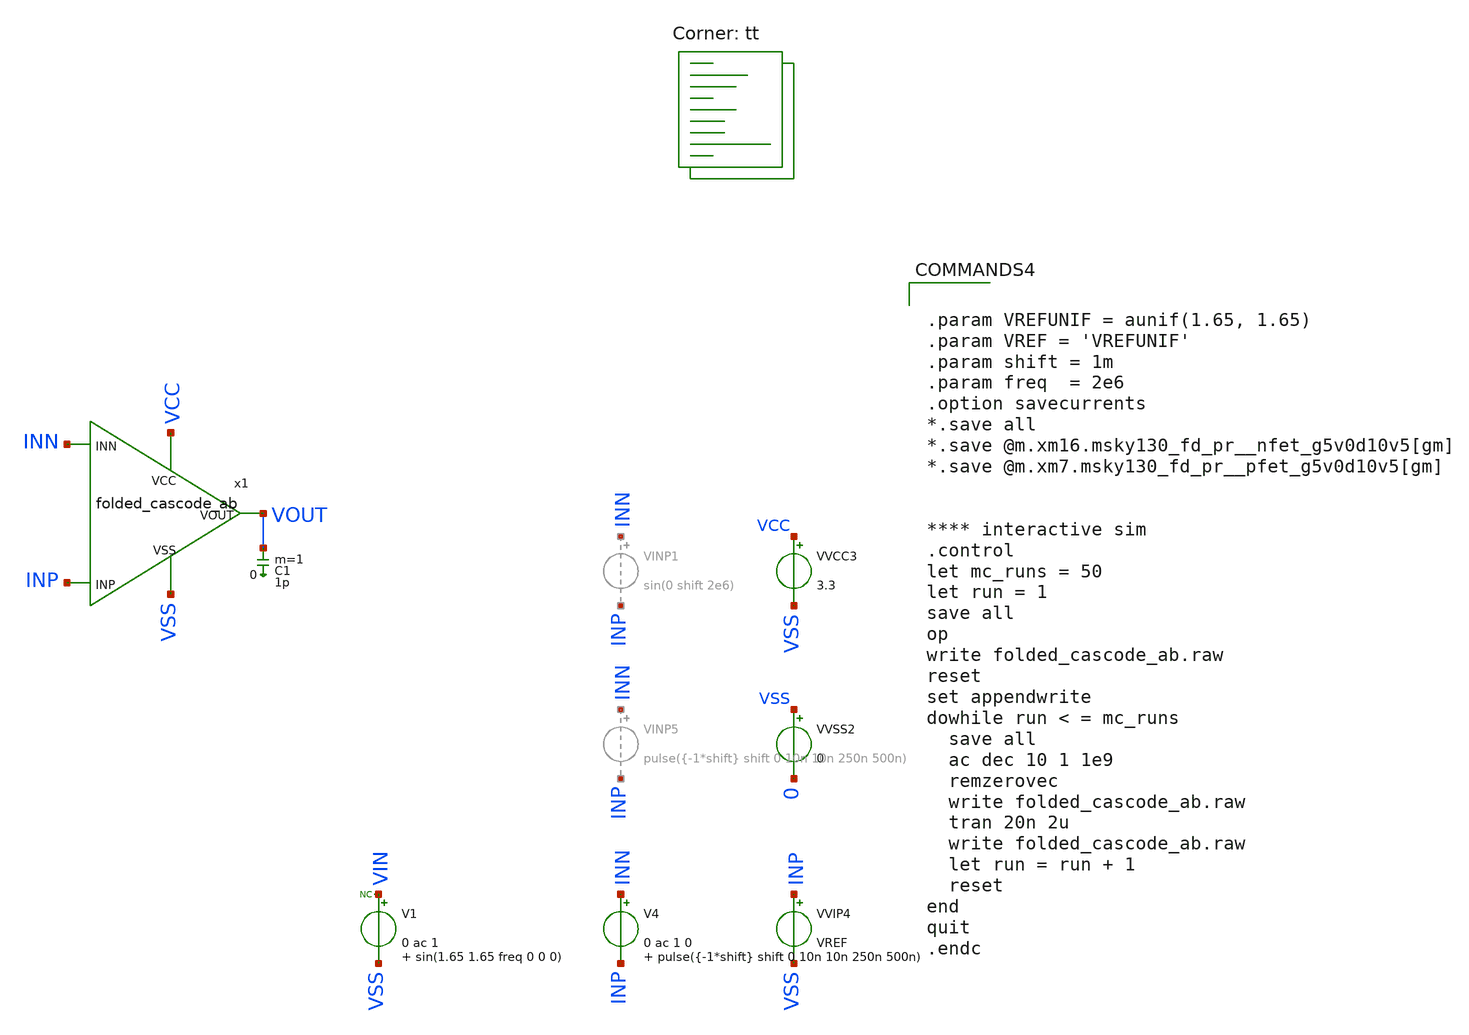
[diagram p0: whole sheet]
** sch_path: cadence_optimized/folded_cascode_ab_tb.sch
**.subckt folded_cascode_ab_tb
VVSS2 VSS 0 0
VVCC3 VCC VSS 3.3
VVIP4 INP VSS VREF
* noconn VIN
V1 VIN VSS 0 ac 1 sin(1.65 1.65 freq 0 0 0)
V4 INN INP 0 ac 1 0 pulse({-1*shift} shift 0 10n 10n 250n 500n)
x1 VSS VCC VOUT INN INP folded_cascode_ab
C1 VOUT 0 1p m=1
**** begin user architecture code
.lib $::SKYWATER_MODELS/sky130.lib.spice tt


.param VREFUNIF = aunif(1.65, 1.65)
.param VREF = 'VREFUNIF'
.param shift = 1m
.param freq  = 2e6
.option savecurrents
*.save all
*.save @m.xm16.msky130_fd_pr__nfet_g5v0d10v5[gm]
*.save @m.xm7.msky130_fd_pr__pfet_g5v0d10v5[gm]


**** interactive sim
.control
let mc_runs = 50
let run = 1
save all
op
write folded_cascode_ab.raw
reset
set appendwrite
dowhile run < = mc_runs
  save all
  ac dec 10 1 1e9
  remzerovec
  write folded_cascode_ab.raw
  tran 20n 2u
  write folded_cascode_ab.raw
  let run = run + 1
  reset
end
quit
.endc




**** end user architecture code
**.ends

* expanding   symbol:
*+  /foss/designs/Comparator/old/schematic/folded_cascode/backup/cadence_optimized/folded_cascode_ab.sym # of pins=5
** sym_path: cadence_optimized/folded_cascode_ab.sym
** sch_path: cadence_optimized/folded_cascode_ab.sch
.subckt folded_cascode_ab VSS VCC VOUT INN INP
*.iopin VCC
*.opin VOUT
*.ipin INN
*.ipin INP
*.iopin VSS
XM1 N4 net3 VSS VSS sky130_fd_pr__nfet_g5v0d10v5 L=0.5 W=4.5 nf=1 ad='int((nf+1)/2) * W/nf * 0.29' as='int((nf+2)/2) * W/nf * 0.29'
+ pd='2*int((nf+1)/2) * (W/nf + 0.29)' ps='2*int((nf+2)/2) * (W/nf + 0.29)' nrd='0.29 / W' nrs='0.29 / W'
+ sa=0 sb=0 sd=0 mult=1 m=1
XM2 out4 y N4 VSS sky130_fd_pr__nfet_g5v0d10v5 L=0.5 W=4 nf=1 ad='int((nf+1)/2) * W/nf * 0.29' as='int((nf+2)/2) * W/nf * 0.29'
+ pd='2*int((nf+1)/2) * (W/nf + 0.29)' ps='2*int((nf+2)/2) * (W/nf + 0.29)' nrd='0.29 / W' nrs='0.29 / W'
+ sa=0 sb=0 sd=0 mult=1 m=1
XM9 net3 y N3 VSS sky130_fd_pr__nfet_g5v0d10v5 L=0.5 W=4 nf=1 ad='int((nf+1)/2) * W/nf * 0.29' as='int((nf+2)/2) * W/nf * 0.29'
+ pd='2*int((nf+1)/2) * (W/nf + 0.29)' ps='2*int((nf+2)/2) * (W/nf + 0.29)' nrd='0.29 / W' nrs='0.29 / W'
+ sa=0 sb=0 sd=0 mult=1 m=1
XM10 N3 net3 VSS VSS sky130_fd_pr__nfet_g5v0d10v5 L=0.5 W=4.5 nf=1 ad='int((nf+1)/2) * W/nf * 0.29' as='int((nf+2)/2) * W/nf * 0.29'
+ pd='2*int((nf+1)/2) * (W/nf + 0.29)' ps='2*int((nf+2)/2) * (W/nf + 0.29)' nrd='0.29 / W' nrs='0.29 / W'
+ sa=0 sb=0 sd=0 mult=1 m=1
XM11 net1 out N1 VCC sky130_fd_pr__pfet_g5v0d10v5 L=0.5 W=4 nf=1 ad='int((nf+1)/2) * W/nf * 0.29' as='int((nf+2)/2) * W/nf * 0.29'
+ pd='2*int((nf+1)/2) * (W/nf + 0.29)' ps='2*int((nf+2)/2) * (W/nf + 0.29)' nrd='0.29 / W' nrs='0.29 / W'
+ sa=0 sb=0 sd=0 mult=1 m=1
XM12 out3 out N2 VCC sky130_fd_pr__pfet_g5v0d10v5 L=0.5 W=4 nf=1 ad='int((nf+1)/2) * W/nf * 0.29' as='int((nf+2)/2) * W/nf * 0.29'
+ pd='2*int((nf+1)/2) * (W/nf + 0.29)' ps='2*int((nf+2)/2) * (W/nf + 0.29)' nrd='0.29 / W' nrs='0.29 / W'
+ sa=0 sb=0 sd=0 mult=1 m=1
XM13 N1 net1 VCC VCC sky130_fd_pr__pfet_g5v0d10v5 L=0.5 W=2 nf=1 ad='int((nf+1)/2) * W/nf * 0.29' as='int((nf+2)/2) * W/nf * 0.29'
+ pd='2*int((nf+1)/2) * (W/nf + 0.29)' ps='2*int((nf+2)/2) * (W/nf + 0.29)' nrd='0.29 / W' nrs='0.29 / W'
+ sa=0 sb=0 sd=0 mult=1 m=1
XM14 N2 net1 VCC VCC sky130_fd_pr__pfet_g5v0d10v5 L=0.5 W=2 nf=1 ad='int((nf+1)/2) * W/nf * 0.29' as='int((nf+2)/2) * W/nf * 0.29'
+ pd='2*int((nf+1)/2) * (W/nf + 0.29)' ps='2*int((nf+2)/2) * (W/nf + 0.29)' nrd='0.29 / W' nrs='0.29 / W'
+ sa=0 sb=0 sd=0 mult=1 m=1
XM16 N2 INN net5 VSS sky130_fd_pr__nfet_g5v0d10v5 L=0.5 W=4 nf=1 ad='int((nf+1)/2) * W/nf * 0.29' as='int((nf+2)/2) * W/nf * 0.29'
+ pd='2*int((nf+1)/2) * (W/nf + 0.29)' ps='2*int((nf+2)/2) * (W/nf + 0.29)' nrd='0.29 / W' nrs='0.29 / W'
+ sa=0 sb=0 sd=0 mult=2 m=2
XM6 N4 INN net2 VCC sky130_fd_pr__pfet_g5v0d10v5 L=0.5 W=4 nf=1 ad='int((nf+1)/2) * W/nf * 0.29' as='int((nf+2)/2) * W/nf * 0.29'
+ pd='2*int((nf+1)/2) * (W/nf + 0.29)' ps='2*int((nf+2)/2) * (W/nf + 0.29)' nrd='0.29 / W' nrs='0.29 / W'
+ sa=0 sb=0 sd=0 mult=2 m=2
Vmeas2 net7 net2 0
.save i(vmeas2)
XM20 s s VCC VCC sky130_fd_pr__pfet_g5v0d10v5 L=0.5 W=0.5 nf=1 ad='int((nf+1)/2) * W/nf * 0.29' as='int((nf+2)/2) * W/nf * 0.29'
+ pd='2*int((nf+1)/2) * (W/nf + 0.29)' ps='2*int((nf+2)/2) * (W/nf + 0.29)' nrd='0.29 / W' nrs='0.29 / W'
+ sa=0 sb=0 sd=0 mult=1 m=1
XM21 p p s VCC sky130_fd_pr__pfet_g5v0d10v5 L=0.5 W=0.5 nf=1 ad='int((nf+1)/2) * W/nf * 0.29' as='int((nf+2)/2) * W/nf * 0.29'
+ pd='2*int((nf+1)/2) * (W/nf + 0.29)' ps='2*int((nf+2)/2) * (W/nf + 0.29)' nrd='0.29 / W' nrs='0.29 / W'
+ sa=0 sb=0 sd=0 mult=1 m=1
XM22 q q net4 VSS sky130_fd_pr__nfet_g5v0d10v5 L=0.5 W=1 nf=1 ad='int((nf+1)/2) * W/nf * 0.29' as='int((nf+2)/2) * W/nf * 0.29'
+ pd='2*int((nf+1)/2) * (W/nf + 0.29)' ps='2*int((nf+2)/2) * (W/nf + 0.29)' nrd='0.29 / W' nrs='0.29 / W'
+ sa=0 sb=0 sd=0 mult=1 m=1
XM23 net4 net4 VSS VSS sky130_fd_pr__nfet_g5v0d10v5 L=0.5 W=1 nf=1 ad='int((nf+1)/2) * W/nf * 0.29' as='int((nf+2)/2) * W/nf * 0.29'
+ pd='2*int((nf+1)/2) * (W/nf + 0.29)' ps='2*int((nf+2)/2) * (W/nf + 0.29)' nrd='0.29 / W' nrs='0.29 / W'
+ sa=0 sb=0 sd=0 mult=1 m=1
XM29 V out3 VCC VCC sky130_fd_pr__pfet_g5v0d10v5 L=2 W=1.5 nf=1 ad='int((nf+1)/2) * W/nf * 0.29' as='int((nf+2)/2) * W/nf * 0.29'
+ pd='2*int((nf+1)/2) * (W/nf + 0.29)' ps='2*int((nf+2)/2) * (W/nf + 0.29)' nrd='0.29 / W' nrs='0.29 / W'
+ sa=0 sb=0 sd=0 mult=1 m=1
XM30 V out4 VSS VSS sky130_fd_pr__nfet_g5v0d10v5 L=2 W=4.1 nf=1 ad='int((nf+1)/2) * W/nf * 0.29' as='int((nf+2)/2) * W/nf * 0.29'
+ pd='2*int((nf+1)/2) * (W/nf + 0.29)' ps='2*int((nf+2)/2) * (W/nf + 0.29)' nrd='0.29 / W' nrs='0.29 / W'
+ sa=0 sb=0 sd=0 mult=1 m=1
XM17 N1 INP net5 VSS sky130_fd_pr__nfet_g5v0d10v5 L=0.5 W=4 nf=1 ad='int((nf+1)/2) * W/nf * 0.29' as='int((nf+2)/2) * W/nf * 0.29'
+ pd='2*int((nf+1)/2) * (W/nf + 0.29)' ps='2*int((nf+2)/2) * (W/nf + 0.29)' nrd='0.29 / W' nrs='0.29 / W'
+ sa=0 sb=0 sd=0 mult=2 m=2
XM3 N3 INP net2 VCC sky130_fd_pr__pfet_g5v0d10v5 L=0.5 W=4 nf=1 ad='int((nf+1)/2) * W/nf * 0.29' as='int((nf+2)/2) * W/nf * 0.29'
+ pd='2*int((nf+1)/2) * (W/nf + 0.29)' ps='2*int((nf+2)/2) * (W/nf + 0.29)' nrd='0.29 / W' nrs='0.29 / W'
+ sa=0 sb=0 sd=0 mult=2 m=2
XM8 out4 p out3 VCC sky130_fd_pr__pfet_g5v0d10v5 L=0.5 W=4 nf=1 ad='int((nf+1)/2) * W/nf * 0.29' as='int((nf+2)/2) * W/nf * 0.29'
+ pd='2*int((nf+1)/2) * (W/nf + 0.29)' ps='2*int((nf+2)/2) * (W/nf + 0.29)' nrd='0.29 / W' nrs='0.29 / W'
+ sa=0 sb=0 sd=0 mult=1 m=1
XM18 net3 p out VCC sky130_fd_pr__pfet_g5v0d10v5 L=0.5 W=4 nf=1 ad='int((nf+1)/2) * W/nf * 0.29' as='int((nf+2)/2) * W/nf * 0.29'
+ pd='2*int((nf+1)/2) * (W/nf + 0.29)' ps='2*int((nf+2)/2) * (W/nf + 0.29)' nrd='0.29 / W' nrs='0.29 / W'
+ sa=0 sb=0 sd=0 mult=1 m=1
XM19 out q net3 VSS sky130_fd_pr__nfet_g5v0d10v5 L=0.5 W=0.5 nf=1 ad='int((nf+1)/2) * W/nf * 0.29' as='int((nf+2)/2) * W/nf * 0.29'
+ pd='2*int((nf+1)/2) * (W/nf + 0.29)' ps='2*int((nf+2)/2) * (W/nf + 0.29)' nrd='0.29 / W' nrs='0.29 / W'
+ sa=0 sb=0 sd=0 mult=1 m=1
XM24 out3 q out4 VSS sky130_fd_pr__nfet_g5v0d10v5 L=0.5 W=0.5 nf=1 ad='int((nf+1)/2) * W/nf * 0.29' as='int((nf+2)/2) * W/nf * 0.29'
+ pd='2*int((nf+1)/2) * (W/nf + 0.29)' ps='2*int((nf+2)/2) * (W/nf + 0.29)' nrd='0.29 / W' nrs='0.29 / W'
+ sa=0 sb=0 sd=0 mult=1 m=1
Vmeas p net9 0
.save i(vmeas)
XM25 x x y VSS sky130_fd_pr__nfet_g5v0d10v5 L=0.5 W=1 nf=1 ad='int((nf+1)/2) * W/nf * 0.29' as='int((nf+2)/2) * W/nf * 0.29'
+ pd='2*int((nf+1)/2) * (W/nf + 0.29)' ps='2*int((nf+2)/2) * (W/nf + 0.29)' nrd='0.29 / W' nrs='0.29 / W'
+ sa=0 sb=0 sd=0 mult=1 m=1
XM26 y y VSS VSS sky130_fd_pr__nfet_g5v0d10v5 L=0.5 W=2.5 nf=1 ad='int((nf+1)/2) * W/nf * 0.29' as='int((nf+2)/2) * W/nf * 0.29'
+ pd='2*int((nf+1)/2) * (W/nf + 0.29)' ps='2*int((nf+2)/2) * (W/nf + 0.29)' nrd='0.29 / W' nrs='0.29 / W'
+ sa=0 sb=0 sd=0 mult=1 m=1
I4 VCC x 30u
XM15 net10 s VCC VCC sky130_fd_pr__pfet_g5v0d10v5 L=0.5 W=0.5 nf=1 ad='int((nf+1)/2) * W/nf * 0.29' as='int((nf+2)/2) * W/nf * 0.29'
+ pd='2*int((nf+1)/2) * (W/nf + 0.29)' ps='2*int((nf+2)/2) * (W/nf + 0.29)' nrd='0.29 / W' nrs='0.29 / W'
+ sa=0 sb=0 sd=0 mult=1 m=1
XM27 net11 p net10 VCC sky130_fd_pr__pfet_g5v0d10v5 L=0.5 W=0.5 nf=1 ad='int((nf+1)/2) * W/nf * 0.29'
+ as='int((nf+2)/2) * W/nf * 0.29' pd='2*int((nf+1)/2) * (W/nf + 0.29)' ps='2*int((nf+2)/2) * (W/nf + 0.29)'
+ nrd='0.29 / W' nrs='0.29 / W' sa=0 sb=0 sd=0 mult=1 m=1
Vmeas1 net11 q 0
.save i(vmeas1)
XM31 net6 y VSS VSS sky130_fd_pr__nfet_g5v0d10v5 L=0.5 W=0.5 nf=1 ad='int((nf+1)/2) * W/nf * 0.29' as='int((nf+2)/2) * W/nf * 0.29'
+ pd='2*int((nf+1)/2) * (W/nf + 0.29)' ps='2*int((nf+2)/2) * (W/nf + 0.29)' nrd='0.29 / W' nrs='0.29 / W'
+ sa=0 sb=0 sd=0 mult=1 m=1
Vmeas3 net5 net6 0
.save i(vmeas3)
XM35 net7 s VCC VCC sky130_fd_pr__pfet_g5v0d10v5 L=0.5 W=0.5 nf=1 ad='int((nf+1)/2) * W/nf * 0.29' as='int((nf+2)/2) * W/nf * 0.29'
+ pd='2*int((nf+1)/2) * (W/nf + 0.29)' ps='2*int((nf+2)/2) * (W/nf + 0.29)' nrd='0.29 / W' nrs='0.29 / W'
+ sa=0 sb=0 sd=0 mult=1 m=1
XR1 out net1 VSS sky130_fd_pr__res_generic_nd__hv W=1 L=264 mult=1 m=1
XM28 net8 V VSS VSS sky130_fd_pr__nfet_g5v0d10v5 L=0.5 W=1 nf=1 ad='int((nf+1)/2) * W/nf * 0.29' as='int((nf+2)/2) * W/nf * 0.29'
+ pd='2*int((nf+1)/2) * (W/nf + 0.29)' ps='2*int((nf+2)/2) * (W/nf + 0.29)' nrd='0.29 / W' nrs='0.29 / W'
+ sa=0 sb=0 sd=0 mult=1 m=1
XM4 net8 s VCC VCC sky130_fd_pr__pfet_g5v0d10v5 L=0.5 W=4 nf=1 ad='int((nf+1)/2) * W/nf * 0.29' as='int((nf+2)/2) * W/nf * 0.29'
+ pd='2*int((nf+1)/2) * (W/nf + 0.29)' ps='2*int((nf+2)/2) * (W/nf + 0.29)' nrd='0.29 / W' nrs='0.29 / W'
+ sa=0 sb=0 sd=0 mult=1 m=1
XM32 net9 x net12 VSS sky130_fd_pr__nfet_g5v0d10v5 L=0.5 W=1 nf=1 ad='int((nf+1)/2) * W/nf * 0.29' as='int((nf+2)/2) * W/nf * 0.29'
+ pd='2*int((nf+1)/2) * (W/nf + 0.29)' ps='2*int((nf+2)/2) * (W/nf + 0.29)' nrd='0.29 / W' nrs='0.29 / W'
+ sa=0 sb=0 sd=0 mult=1 m=1
XM33 net12 y VSS VSS sky130_fd_pr__nfet_g5v0d10v5 L=0.5 W=2.5 nf=1 ad='int((nf+1)/2) * W/nf * 0.29' as='int((nf+2)/2) * W/nf * 0.29'
+ pd='2*int((nf+1)/2) * (W/nf + 0.29)' ps='2*int((nf+2)/2) * (W/nf + 0.29)' nrd='0.29 / W' nrs='0.29 / W'
+ sa=0 sb=0 sd=0 mult=1 m=1
XM5 VOUT net8 VSS VSS sky130_fd_pr__nfet_g5v0d10v5 L=0.5 W=1 nf=1 ad='int((nf+1)/2) * W/nf * 0.29' as='int((nf+2)/2) * W/nf * 0.29'
+ pd='2*int((nf+1)/2) * (W/nf + 0.29)' ps='2*int((nf+2)/2) * (W/nf + 0.29)' nrd='0.29 / W' nrs='0.29 / W'
+ sa=0 sb=0 sd=0 mult=1 m=1
XM7 VOUT net8 VCC VCC sky130_fd_pr__pfet_g5v0d10v5 L=0.5 W=4 nf=1 ad='int((nf+1)/2) * W/nf * 0.29' as='int((nf+2)/2) * W/nf * 0.29'
+ pd='2*int((nf+1)/2) * (W/nf + 0.29)' ps='2*int((nf+2)/2) * (W/nf + 0.29)' nrd='0.29 / W' nrs='0.29 / W'
+ sa=0 sb=0 sd=0 mult=1 m=1
.ends

.end
